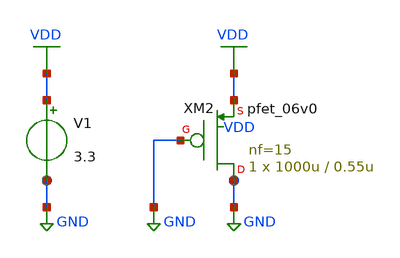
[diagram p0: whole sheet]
** sch_path: tb_test.sch
**.subckt tb_test
V1 VDD GND 3.3
XM2 GND GND VDD VDD pfet_06v0 L=0.55u W=1000u nf=15 ad='int((nf+1)/2) * W/nf * 0.18u' as='int((nf+2)/2) * W/nf * 0.18u'
+ pd='2*int((nf+1)/2) * (W/nf + 0.18u)' ps='2*int((nf+2)/2) * (W/nf + 0.18u)' nrd='0.18u / W' nrs='0.18u / W'
+ sa=0 sb=0 sd=0 m=1 par=1
**** begin user architecture code


.control
op
.endc
.end



.include design.ngspice
.lib sm141064.ngspice typical

**** end user architecture code
**.ends
.GLOBAL GND
.GLOBAL VDD
.end
